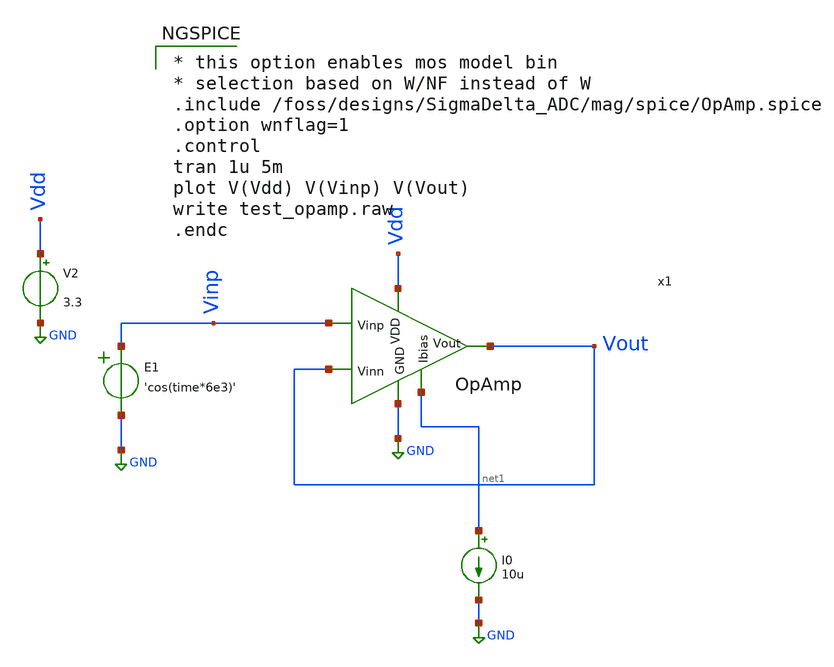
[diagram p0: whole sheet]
** sch_path: xschem/OpAmp_v0/OpAmp_tb.sch
**.subckt OpAmp_tb
V2 Vdd GND 3.3
I0 net1 GND 10u
E1 Vinp GND VOL=' 'cos(time*6e3)' '
x1 Vdd Vout net1 Vout Vinp GND OpAmp
**** begin user architecture code

* this option enables mos model bin
* selection based on W/NF instead of W
.include /foss/designs/SigmaDelta_ADC/mag/spice/OpAmp.spice
.option wnflag=1
.control
tran 1u 5m
plot V(Vdd) V(Vinp) V(Vout)
write test_opamp.raw
.endc


.lib /foss/designs/PDK/sky130B/libs.tech/ngspice/sky130.lib.spice tt
.include /foss/designs/PDK/sky130B/libs.ref/sky130_fd_sc_hvl/spice/sky130_fd_sc_hvl.spice

**** end user architecture code
**.ends
.GLOBAL GND
.end
